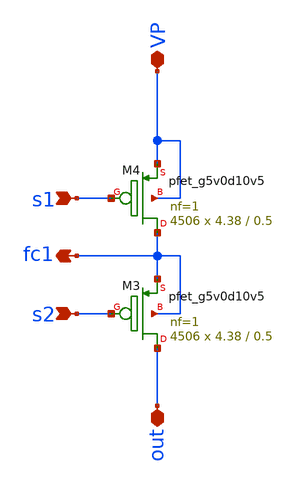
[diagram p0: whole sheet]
** sch_path: xschem/hierarchy_sch/transistor_group_one.sch
**.subckt transistor_group_one VP s1 s2 fc1 out
*.iopin VP
*.ipin s1
*.ipin s2
*.opin fc1
*.iopin out
XM3 out s2 fc1 fc1 sky130_fd_pr__pfet_g5v0d10v5 L=0.5 W=4.38 nf=1 ad='int((nf+1)/2) * W/nf * 0.29' as='int((nf+2)/2) * W/nf * 0.29'
+ pd='2*int((nf+1)/2) * (W/nf + 0.29)' ps='2*int((nf+2)/2) * (W/nf + 0.29)' nrd='0.29 / W' nrs='0.29 / W'
+ sa=0 sb=0 sd=0 mult=4506 m=4506
XM4 fc1 s1 VP VP sky130_fd_pr__pfet_g5v0d10v5 L=0.5 W=4.38 nf=1 ad='int((nf+1)/2) * W/nf * 0.29' as='int((nf+2)/2) * W/nf * 0.29'
+ pd='2*int((nf+1)/2) * (W/nf + 0.29)' ps='2*int((nf+2)/2) * (W/nf + 0.29)' nrd='0.29 / W' nrs='0.29 / W'
+ sa=0 sb=0 sd=0 mult=4506 m=4506
**.ends
.end
